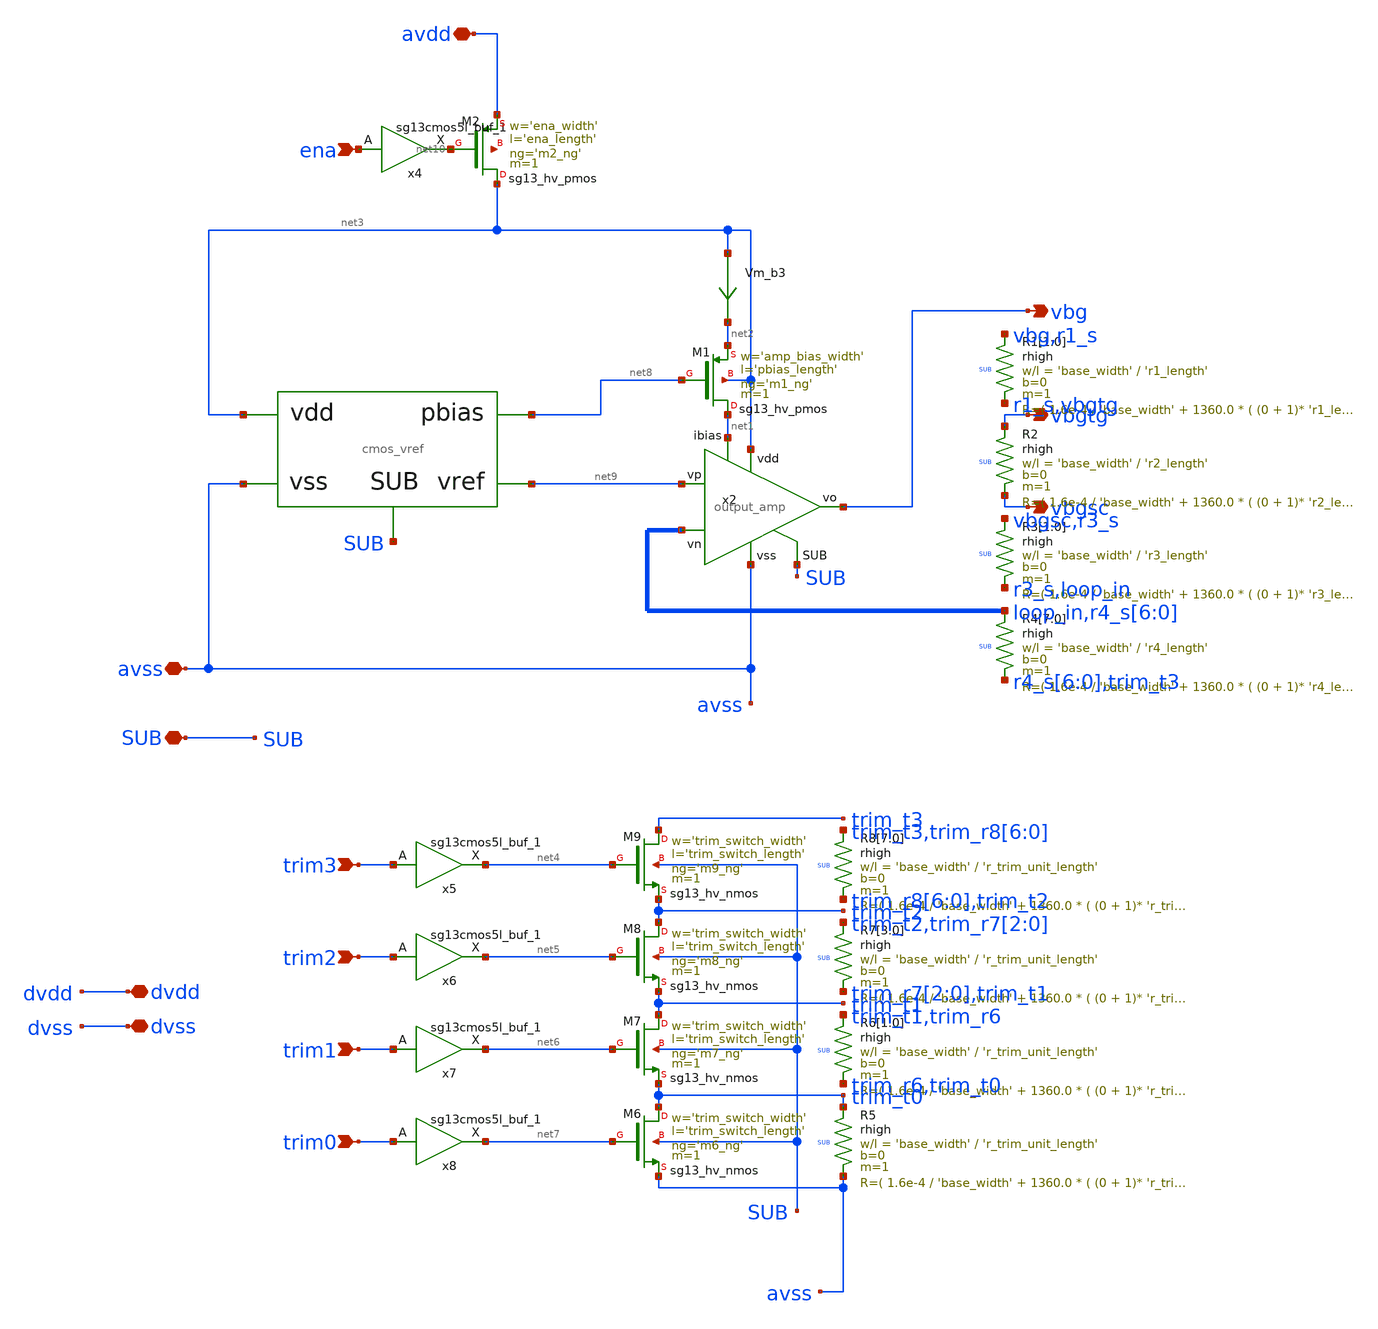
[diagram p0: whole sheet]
** sch_path: sch/top/top_default.sch
**.subckt top_default vbg avss SUB dvdd dvss vbgsc vbgtg trim3 trim2 trim1 trim0 avdd ena
*.opin vbg
*.iopin avss
*.iopin SUB
*.iopin dvdd
*.iopin dvss
*.opin vbgsc
*.opin vbgtg
*.ipin trim3
*.ipin trim2
*.ipin trim1
*.ipin trim0
*.iopin avdd
*.ipin ena
x2 net3 vbg net9 loop_in net1 avss SUB output_amp
Vm_b3 net3 net2 0
.save i(vm_b3)
XM1 net1 net8 net2 net3 sg13_hv_pmos w='amp_bias_width' l='pbias_length' ng='m1_ng' m=1 mm_ok=1
x5 net4 trim3 dvdd dvss sg13cmos5l_buf_1
x6 net5 trim2 dvdd dvss sg13cmos5l_buf_1
x7 net6 trim1 dvdd dvss sg13cmos5l_buf_1
x8 net7 trim0 dvdd dvss sg13cmos5l_buf_1
XR1[1] vbg r1_s SUB rhigh w='base_width' l='r1_length' m=1 b=0 mm_ok=1
XR1[0] r1_s vbgtg SUB rhigh w='base_width' l='r1_length' m=1 b=0 mm_ok=1
XR2 vbgtg vbgsc SUB rhigh w='base_width' l='r2_length' m=1 b=0 mm_ok=1
XR3[1] vbgsc r3_s SUB rhigh w='base_width' l='r3_length' m=1 b=0 mm_ok=1
XR3[0] r3_s loop_in SUB rhigh w='base_width' l='r3_length' m=1 b=0 mm_ok=1
XR4[7] loop_in r4_s[6] SUB rhigh w='base_width' l='r4_length' m=1 b=0 mm_ok=1
XR4[6] r4_s[6] r4_s[5] SUB rhigh w='base_width' l='r4_length' m=1 b=0 mm_ok=1
XR4[5] r4_s[5] r4_s[4] SUB rhigh w='base_width' l='r4_length' m=1 b=0 mm_ok=1
XR4[4] r4_s[4] r4_s[3] SUB rhigh w='base_width' l='r4_length' m=1 b=0 mm_ok=1
XR4[3] r4_s[3] r4_s[2] SUB rhigh w='base_width' l='r4_length' m=1 b=0 mm_ok=1
XR4[2] r4_s[2] r4_s[1] SUB rhigh w='base_width' l='r4_length' m=1 b=0 mm_ok=1
XR4[1] r4_s[1] r4_s[0] SUB rhigh w='base_width' l='r4_length' m=1 b=0 mm_ok=1
XR4[0] r4_s[0] trim_t3 SUB rhigh w='base_width' l='r4_length' m=1 b=0 mm_ok=1
XM6 trim_t0 net7 avss SUB sg13_hv_nmos w='trim_switch_width' l='trim_switch_length' ng='m6_ng' m=1 mm_ok=1
XM7 trim_t1 net6 trim_t0 SUB sg13_hv_nmos w='trim_switch_width' l='trim_switch_length' ng='m7_ng' m=1
+ mm_ok=1
XM8 trim_t2 net5 trim_t1 SUB sg13_hv_nmos w='trim_switch_width' l='trim_switch_length' ng='m8_ng' m=1
+ mm_ok=1
XM9 trim_t3 net4 trim_t2 SUB sg13_hv_nmos w='trim_switch_width' l='trim_switch_length' ng='m9_ng' m=1
+ mm_ok=1
XR5 trim_t0 avss SUB rhigh w='base_width' l='r_trim_unit_length' m=1 b=0 mm_ok=1
XR6[1] trim_t1 trim_r6 SUB rhigh w='base_width' l='r_trim_unit_length' m=1 b=0 mm_ok=1
XR6[0] trim_r6 trim_t0 SUB rhigh w='base_width' l='r_trim_unit_length' m=1 b=0 mm_ok=1
XR7[3] trim_t2 trim_r7[2] SUB rhigh w='base_width' l='r_trim_unit_length' m=1 b=0 mm_ok=1
XR7[2] trim_r7[2] trim_r7[1] SUB rhigh w='base_width' l='r_trim_unit_length' m=1 b=0 mm_ok=1
XR7[1] trim_r7[1] trim_r7[0] SUB rhigh w='base_width' l='r_trim_unit_length' m=1 b=0 mm_ok=1
XR7[0] trim_r7[0] trim_t1 SUB rhigh w='base_width' l='r_trim_unit_length' m=1 b=0 mm_ok=1
XR8[7] trim_t3 trim_r8[6] SUB rhigh w='base_width' l='r_trim_unit_length' m=1 b=0 mm_ok=1
XR8[6] trim_r8[6] trim_r8[5] SUB rhigh w='base_width' l='r_trim_unit_length' m=1 b=0 mm_ok=1
XR8[5] trim_r8[5] trim_r8[4] SUB rhigh w='base_width' l='r_trim_unit_length' m=1 b=0 mm_ok=1
XR8[4] trim_r8[4] trim_r8[3] SUB rhigh w='base_width' l='r_trim_unit_length' m=1 b=0 mm_ok=1
XR8[3] trim_r8[3] trim_r8[2] SUB rhigh w='base_width' l='r_trim_unit_length' m=1 b=0 mm_ok=1
XR8[2] trim_r8[2] trim_r8[1] SUB rhigh w='base_width' l='r_trim_unit_length' m=1 b=0 mm_ok=1
XR8[1] trim_r8[1] trim_r8[0] SUB rhigh w='base_width' l='r_trim_unit_length' m=1 b=0 mm_ok=1
XR8[0] trim_r8[0] trim_t2 SUB rhigh w='base_width' l='r_trim_unit_length' m=1 b=0 mm_ok=1
X1 net9 net3 avss net8 SUB cmos_vref
x4 net10 ena dvdd dvss sg13cmos5l_buf_1
XM2 net3 net10 avdd net11 sg13_hv_pmos w='ena_width' l='ena_length' ng='m2_ng' m=1 mm_ok=1
**.ends
.end
